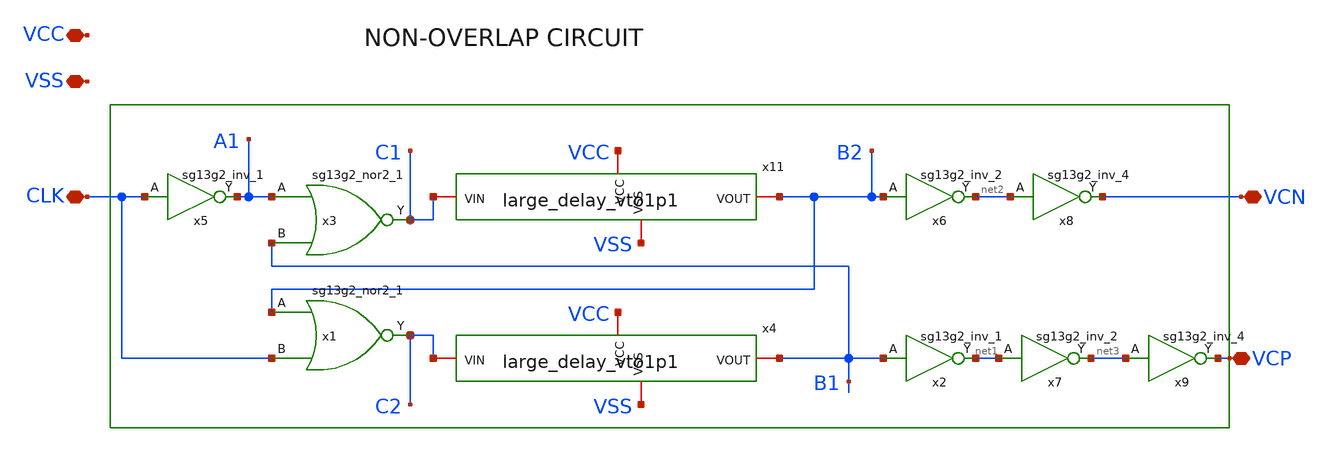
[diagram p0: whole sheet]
** sch_path: AC3E_USM_TDBUCK/design_data/xschem/NOL/NOL_vto1p1.sch
* IHP-GmbH/IHP-Open-PDK/ihp-sg13g2/libs.tech/xschem/sg13g2_stdcells/sg13g2_inv_2.sch:
* Copyright 2023 IHP PDK Authors
* Licensed under the Apache License, Version 2.0 (the "License");
**.subckt NOL_vto1p1 CLK VCP VCN VCC VSS
*.iopin CLK
*.iopin VCP
*.iopin VCN
*.iopin VCC
*.iopin VSS
x5 A1 CLK VCC VSS sg13g2_inv_1
x3 C1 A1 B1 VCC VSS sg13g2_nor2_1
x1 C2 B2 CLK VCC VSS sg13g2_nor2_1
x2 net1 B1 VCC VSS sg13g2_inv_1
x6 net2 B2 VCC VSS sg13g2_inv_2
x7 net3 net1 VCC VSS sg13g2_inv_2
x8 VCN net2 VCC VSS sg13g2_inv_4
x9 VCP net3 VCC VSS sg13g2_inv_4
x11 VCC VSS C1 B2 large_delay_vto1p1
x4 VCC VSS C2 B1 large_delay_vto1p1
**.ends

* expanding   symbol:  sg13g2_stdcells/sg13g2_inv_1.sym # of pins=2
** sym_path: sg13g2_stdcells/sg13g2_inv_1.sym
** sch_path: sg13g2_stdcells/sg13g2_inv_1.sch
.subckt sg13g2_inv_1 Y A VDD VSS
*.opin Y
*.ipin A
*.iopin VDD
*.iopin VSS
XM1 Y A VSS VSS sg13_lv_nmos w=740.00n l=130.00n ng=1 m=1 mm_ok=1
XM2 Y A VDD VDD sg13_lv_pmos w=1.12u l=130.00n ng=1 m=1 mm_ok=1
.ends


* expanding   symbol:  sg13g2_stdcells/sg13g2_nor2_1.sym # of pins=3
** sym_path: sg13g2_stdcells/sg13g2_nor2_1.sym
** sch_path: sg13g2_stdcells/sg13g2_nor2_1.sch
.subckt sg13g2_nor2_1 Y A B VDD VSS
*.opin Y
*.ipin B
*.ipin A
*.iopin VDD
*.iopin VSS
XM1 Y A VSS VSS sg13_lv_nmos w=740.00n l=130.00n ng=1 m=1 mm_ok=1
XM2 Y B VSS VSS sg13_lv_nmos w=740.00n l=130.00n ng=1 m=1 mm_ok=1
XM3 net1 A VDD VDD sg13_lv_pmos w=1.12u l=130.00n ng=1 m=1 mm_ok=1
XM4 Y B net1 VDD sg13_lv_pmos w=1.12u l=130.00n ng=1 m=1 mm_ok=1
.ends


* expanding   symbol:  sg13g2_stdcells/sg13g2_inv_2.sym # of pins=2
** sym_path: sg13g2_stdcells/sg13g2_inv_2.sym
** sch_path: sg13g2_stdcells/sg13g2_inv_2.sch
.subckt sg13g2_inv_2 Y A VDD VSS
*.opin Y
*.ipin A
*.iopin VDD
*.iopin VSS
XM1 Y A VSS VSS sg13_lv_nmos w=1.48u l=130.00n ng=2 m=1 mm_ok=1
XM2 Y A VDD VDD sg13_lv_pmos w=2.24u l=130.00n ng=2 m=1 mm_ok=1
.ends


* expanding   symbol:  sg13g2_stdcells/sg13g2_inv_4.sym # of pins=2
** sym_path: sg13g2_stdcells/sg13g2_inv_4.sym
** sch_path: sg13g2_stdcells/sg13g2_inv_4.sch
.subckt sg13g2_inv_4 Y A VDD VSS
*.ipin A
*.opin Y
*.iopin VDD
*.iopin VSS
XM1 Y A VSS VSS sg13_lv_nmos w=2.96u l=130.00n ng=4 m=1 mm_ok=1
XM2 Y A VDD VDD sg13_lv_pmos w=4.48u l=130.00n ng=4 m=1 mm_ok=1
.ends


* expanding   symbol:  ../large_delay/large_delay_vto1p1.sym # of pins=4
** sym_path: ../large_delay/large_delay_vto1p1.sym
** sch_path: ../large_delay/large_delay_vto1p1.sch
.subckt large_delay_vto1p1 VCC VSS VIN VOUT
*.iopin VIN
*.iopin VOUT
*.iopin VCC
*.iopin VSS
x1[0] n2 VIN VCC VSS sg13g2_dlygate4sd3_1
x1[1] n3 n2 VCC VSS sg13g2_dlygate4sd3_1
x1[2] n4 n3 VCC VSS sg13g2_dlygate4sd3_1
x1[3] n5 n4 VCC VSS sg13g2_dlygate4sd3_1
x1[4] VOUT n5 VCC VSS sg13g2_dlygate4sd3_1
.ends


* expanding   symbol:  sg13g2_stdcells/sg13g2_dlygate4sd3_1.sym # of pins=2
** sym_path: sg13g2_stdcells/sg13g2_dlygate4sd3_1.sym
** sch_path: sg13g2_stdcells/sg13g2_dlygate4sd3_1.sch
.subckt sg13g2_dlygate4sd3_1 X A VDD VSS
*.ipin A
*.opin X
*.iopin VDD
*.iopin VSS
XM1 net3 A VSS VSS sg13_lv_nmos w=420.00n l=130.00n ng=1 m=1 mm_ok=1
XM2 net1 net3 VSS VSS sg13_lv_nmos w=420.00n l=500.0n ng=1 m=1 mm_ok=1
XM3 net2 net1 VSS VSS sg13_lv_nmos w=420.00n l=500.0n ng=1 m=1 mm_ok=1
XM4 X net2 VSS VSS sg13_lv_nmos w=740.00n l=130.00n ng=1 m=1 mm_ok=1
XM5 net3 A VDD VDD sg13_lv_pmos w=420.00n l=130.00n ng=1 m=1 mm_ok=1
XM6 net1 net3 VDD VDD sg13_lv_pmos w=1.000u l=500.0n ng=1 m=1 mm_ok=1
XM7 net2 net1 VDD VDD sg13_lv_pmos w=1.000u l=500.0n ng=1 m=1 mm_ok=1
XM8 X net2 VDD VDD sg13_lv_pmos w=1.12u l=130.00n ng=1 m=1 mm_ok=1
.ends

.end
